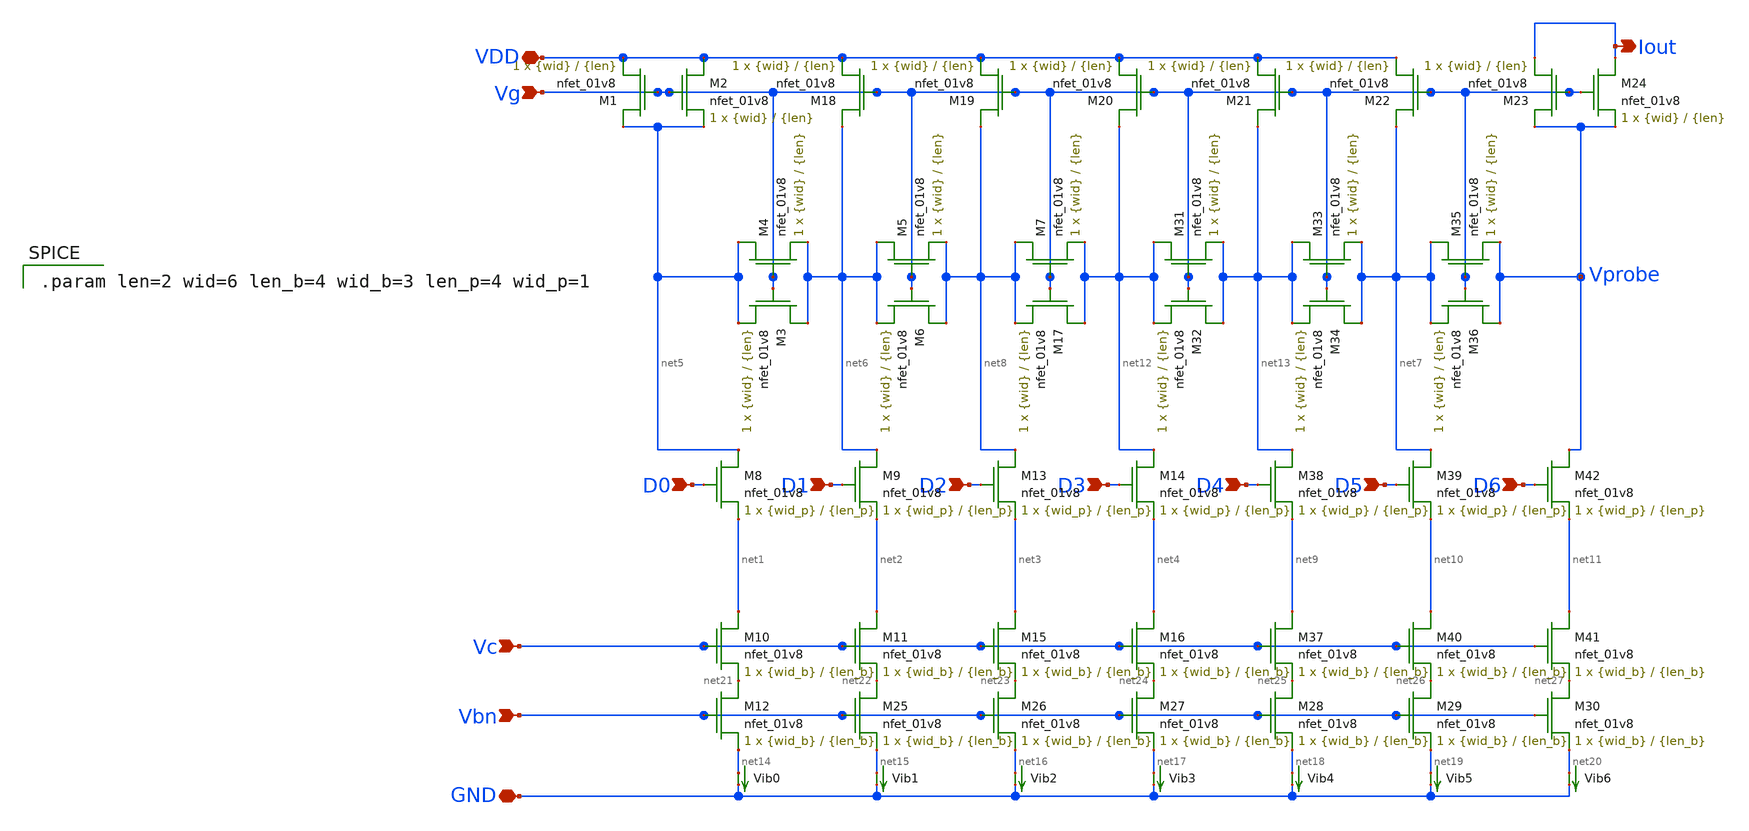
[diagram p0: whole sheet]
** sch_path: mp3/ladder.sch
**.subckt ladder Vbn VDD Iout GND D0 D1 D2 D3 D4 D5 D6 Vg Vc
*.ipin Vbn
*.iopin VDD
*.opin Iout
*.iopin GND
*.ipin D0
*.ipin D1
*.ipin D2
*.ipin D3
*.ipin D4
*.ipin D5
*.ipin D6
*.ipin Vg
*.ipin Vc
XM1 net5 Vg VDD GND sky130_fd_pr__nfet_01v8 L={len} W={wid} nf=1 ad='int((nf+1)/2) * W/nf * 0.29' as='int((nf+2)/2) * W/nf * 0.29'
+ pd='2*int((nf+1)/2) * (W/nf + 0.29)' ps='2*int((nf+2)/2) * (W/nf + 0.29)' nrd='0.29 / W' nrs='0.29 / W'
+ sa=0 sb=0 sd=0 mult=1 m=1
XM4 net5 Vg net6 GND sky130_fd_pr__nfet_01v8 L={len} W={wid} nf=1 ad='int((nf+1)/2) * W/nf * 0.29' as='int((nf+2)/2) * W/nf * 0.29'
+ pd='2*int((nf+1)/2) * (W/nf + 0.29)' ps='2*int((nf+2)/2) * (W/nf + 0.29)' nrd='0.29 / W' nrs='0.29 / W'
+ sa=0 sb=0 sd=0 mult=1 m=1
XM12 net21 Vbn net14 GND sky130_fd_pr__nfet_01v8 L={len_b} W={wid_b} nf=1 ad='int((nf+1)/2) * W/nf * 0.29'
+ as='int((nf+2)/2) * W/nf * 0.29' pd='2*int((nf+1)/2) * (W/nf + 0.29)' ps='2*int((nf+2)/2) * (W/nf + 0.29)'
+ nrd='0.29 / W' nrs='0.29 / W' sa=0 sb=0 sd=0 mult=1 m=1
XM2 VDD Vg net5 GND sky130_fd_pr__nfet_01v8 L={len} W={wid} nf=1 ad='int((nf+1)/2) * W/nf * 0.29' as='int((nf+2)/2) * W/nf * 0.29'
+ pd='2*int((nf+1)/2) * (W/nf + 0.29)' ps='2*int((nf+2)/2) * (W/nf + 0.29)' nrd='0.29 / W' nrs='0.29 / W'
+ sa=0 sb=0 sd=0 mult=1 m=1
XM18 net6 Vg VDD GND sky130_fd_pr__nfet_01v8 L={len} W={wid} nf=1 ad='int((nf+1)/2) * W/nf * 0.29' as='int((nf+2)/2) * W/nf * 0.29'
+ pd='2*int((nf+1)/2) * (W/nf + 0.29)' ps='2*int((nf+2)/2) * (W/nf + 0.29)' nrd='0.29 / W' nrs='0.29 / W'
+ sa=0 sb=0 sd=0 mult=1 m=1
XM19 net8 Vg VDD GND sky130_fd_pr__nfet_01v8 L={len} W={wid} nf=1 ad='int((nf+1)/2) * W/nf * 0.29' as='int((nf+2)/2) * W/nf * 0.29'
+ pd='2*int((nf+1)/2) * (W/nf + 0.29)' ps='2*int((nf+2)/2) * (W/nf + 0.29)' nrd='0.29 / W' nrs='0.29 / W'
+ sa=0 sb=0 sd=0 mult=1 m=1
XM20 net12 Vg VDD GND sky130_fd_pr__nfet_01v8 L={len} W={wid} nf=1 ad='int((nf+1)/2) * W/nf * 0.29' as='int((nf+2)/2) * W/nf * 0.29'
+ pd='2*int((nf+1)/2) * (W/nf + 0.29)' ps='2*int((nf+2)/2) * (W/nf + 0.29)' nrd='0.29 / W' nrs='0.29 / W'
+ sa=0 sb=0 sd=0 mult=1 m=1
XM21 net13 Vg VDD GND sky130_fd_pr__nfet_01v8 L={len} W={wid} nf=1 ad='int((nf+1)/2) * W/nf * 0.29' as='int((nf+2)/2) * W/nf * 0.29'
+ pd='2*int((nf+1)/2) * (W/nf + 0.29)' ps='2*int((nf+2)/2) * (W/nf + 0.29)' nrd='0.29 / W' nrs='0.29 / W'
+ sa=0 sb=0 sd=0 mult=1 m=1
XM22 net7 Vg VDD GND sky130_fd_pr__nfet_01v8 L={len} W={wid} nf=1 ad='int((nf+1)/2) * W/nf * 0.29' as='int((nf+2)/2) * W/nf * 0.29'
+ pd='2*int((nf+1)/2) * (W/nf + 0.29)' ps='2*int((nf+2)/2) * (W/nf + 0.29)' nrd='0.29 / W' nrs='0.29 / W'
+ sa=0 sb=0 sd=0 mult=1 m=1
XM23 Vprobe Vg Iout GND sky130_fd_pr__nfet_01v8 L={len} W={wid} nf=1 ad='int((nf+1)/2) * W/nf * 0.29'
+ as='int((nf+2)/2) * W/nf * 0.29' pd='2*int((nf+1)/2) * (W/nf + 0.29)' ps='2*int((nf+2)/2) * (W/nf + 0.29)'
+ nrd='0.29 / W' nrs='0.29 / W' sa=0 sb=0 sd=0 mult=1 m=1
XM24 Iout Vg Vprobe GND sky130_fd_pr__nfet_01v8 L={len} W={wid} nf=1 ad='int((nf+1)/2) * W/nf * 0.29'
+ as='int((nf+2)/2) * W/nf * 0.29' pd='2*int((nf+1)/2) * (W/nf + 0.29)' ps='2*int((nf+2)/2) * (W/nf + 0.29)'
+ nrd='0.29 / W' nrs='0.29 / W' sa=0 sb=0 sd=0 mult=1 m=1
XM3 net6 Vg net5 GND sky130_fd_pr__nfet_01v8 L={len} W={wid} nf=1 ad='int((nf+1)/2) * W/nf * 0.29' as='int((nf+2)/2) * W/nf * 0.29'
+ pd='2*int((nf+1)/2) * (W/nf + 0.29)' ps='2*int((nf+2)/2) * (W/nf + 0.29)' nrd='0.29 / W' nrs='0.29 / W'
+ sa=0 sb=0 sd=0 mult=1 m=1
XM5 net6 Vg net8 GND sky130_fd_pr__nfet_01v8 L={len} W={wid} nf=1 ad='int((nf+1)/2) * W/nf * 0.29' as='int((nf+2)/2) * W/nf * 0.29'
+ pd='2*int((nf+1)/2) * (W/nf + 0.29)' ps='2*int((nf+2)/2) * (W/nf + 0.29)' nrd='0.29 / W' nrs='0.29 / W'
+ sa=0 sb=0 sd=0 mult=1 m=1
XM6 net8 Vg net6 GND sky130_fd_pr__nfet_01v8 L={len} W={wid} nf=1 ad='int((nf+1)/2) * W/nf * 0.29' as='int((nf+2)/2) * W/nf * 0.29'
+ pd='2*int((nf+1)/2) * (W/nf + 0.29)' ps='2*int((nf+2)/2) * (W/nf + 0.29)' nrd='0.29 / W' nrs='0.29 / W'
+ sa=0 sb=0 sd=0 mult=1 m=1
XM7 net8 Vg net12 GND sky130_fd_pr__nfet_01v8 L={len} W={wid} nf=1 ad='int((nf+1)/2) * W/nf * 0.29' as='int((nf+2)/2) * W/nf * 0.29'
+ pd='2*int((nf+1)/2) * (W/nf + 0.29)' ps='2*int((nf+2)/2) * (W/nf + 0.29)' nrd='0.29 / W' nrs='0.29 / W'
+ sa=0 sb=0 sd=0 mult=1 m=1
XM17 net12 Vg net8 GND sky130_fd_pr__nfet_01v8 L={len} W={wid} nf=1 ad='int((nf+1)/2) * W/nf * 0.29'
+ as='int((nf+2)/2) * W/nf * 0.29' pd='2*int((nf+1)/2) * (W/nf + 0.29)' ps='2*int((nf+2)/2) * (W/nf + 0.29)'
+ nrd='0.29 / W' nrs='0.29 / W' sa=0 sb=0 sd=0 mult=1 m=1
XM31 net12 Vg net13 GND sky130_fd_pr__nfet_01v8 L={len} W={wid} nf=1 ad='int((nf+1)/2) * W/nf * 0.29'
+ as='int((nf+2)/2) * W/nf * 0.29' pd='2*int((nf+1)/2) * (W/nf + 0.29)' ps='2*int((nf+2)/2) * (W/nf + 0.29)'
+ nrd='0.29 / W' nrs='0.29 / W' sa=0 sb=0 sd=0 mult=1 m=1
XM32 net13 Vg net12 GND sky130_fd_pr__nfet_01v8 L={len} W={wid} nf=1 ad='int((nf+1)/2) * W/nf * 0.29'
+ as='int((nf+2)/2) * W/nf * 0.29' pd='2*int((nf+1)/2) * (W/nf + 0.29)' ps='2*int((nf+2)/2) * (W/nf + 0.29)'
+ nrd='0.29 / W' nrs='0.29 / W' sa=0 sb=0 sd=0 mult=1 m=1
XM33 net13 Vg net7 GND sky130_fd_pr__nfet_01v8 L={len} W={wid} nf=1 ad='int((nf+1)/2) * W/nf * 0.29'
+ as='int((nf+2)/2) * W/nf * 0.29' pd='2*int((nf+1)/2) * (W/nf + 0.29)' ps='2*int((nf+2)/2) * (W/nf + 0.29)'
+ nrd='0.29 / W' nrs='0.29 / W' sa=0 sb=0 sd=0 mult=1 m=1
XM34 net7 Vg net13 GND sky130_fd_pr__nfet_01v8 L={len} W={wid} nf=1 ad='int((nf+1)/2) * W/nf * 0.29'
+ as='int((nf+2)/2) * W/nf * 0.29' pd='2*int((nf+1)/2) * (W/nf + 0.29)' ps='2*int((nf+2)/2) * (W/nf + 0.29)'
+ nrd='0.29 / W' nrs='0.29 / W' sa=0 sb=0 sd=0 mult=1 m=1
XM35 net7 Vg Vprobe GND sky130_fd_pr__nfet_01v8 L={len} W={wid} nf=1 ad='int((nf+1)/2) * W/nf * 0.29'
+ as='int((nf+2)/2) * W/nf * 0.29' pd='2*int((nf+1)/2) * (W/nf + 0.29)' ps='2*int((nf+2)/2) * (W/nf + 0.29)'
+ nrd='0.29 / W' nrs='0.29 / W' sa=0 sb=0 sd=0 mult=1 m=1
XM36 Vprobe Vg net7 GND sky130_fd_pr__nfet_01v8 L={len} W={wid} nf=1 ad='int((nf+1)/2) * W/nf * 0.29'
+ as='int((nf+2)/2) * W/nf * 0.29' pd='2*int((nf+1)/2) * (W/nf + 0.29)' ps='2*int((nf+2)/2) * (W/nf + 0.29)'
+ nrd='0.29 / W' nrs='0.29 / W' sa=0 sb=0 sd=0 mult=1 m=1
Vib0 net14 GND 0
.save i(vib0)
Vib1 net15 GND 0
.save i(vib1)
Vib2 net16 GND 0
.save i(vib2)
Vib3 net17 GND 0
.save i(vib3)
Vib4 net18 GND 0
.save i(vib4)
Vib5 net19 GND 0
.save i(vib5)
Vib6 net20 GND 0
.save i(vib6)
XM8 net5 D0 net1 GND sky130_fd_pr__nfet_01v8 L={len_p} W={wid_p} nf=1 ad='int((nf+1)/2) * W/nf * 0.29'
+ as='int((nf+2)/2) * W/nf * 0.29' pd='2*int((nf+1)/2) * (W/nf + 0.29)' ps='2*int((nf+2)/2) * (W/nf + 0.29)'
+ nrd='0.29 / W' nrs='0.29 / W' sa=0 sb=0 sd=0 mult=1 m=1
XM9 net6 D1 net2 GND sky130_fd_pr__nfet_01v8 L={len_p} W={wid_p} nf=1 ad='int((nf+1)/2) * W/nf * 0.29'
+ as='int((nf+2)/2) * W/nf * 0.29' pd='2*int((nf+1)/2) * (W/nf + 0.29)' ps='2*int((nf+2)/2) * (W/nf + 0.29)'
+ nrd='0.29 / W' nrs='0.29 / W' sa=0 sb=0 sd=0 mult=1 m=1
XM13 net8 D2 net3 GND sky130_fd_pr__nfet_01v8 L={len_p} W={wid_p} nf=1 ad='int((nf+1)/2) * W/nf * 0.29'
+ as='int((nf+2)/2) * W/nf * 0.29' pd='2*int((nf+1)/2) * (W/nf + 0.29)' ps='2*int((nf+2)/2) * (W/nf + 0.29)'
+ nrd='0.29 / W' nrs='0.29 / W' sa=0 sb=0 sd=0 mult=1 m=1
XM14 net12 D3 net4 GND sky130_fd_pr__nfet_01v8 L={len_p} W={wid_p} nf=1 ad='int((nf+1)/2) * W/nf * 0.29'
+ as='int((nf+2)/2) * W/nf * 0.29' pd='2*int((nf+1)/2) * (W/nf + 0.29)' ps='2*int((nf+2)/2) * (W/nf + 0.29)'
+ nrd='0.29 / W' nrs='0.29 / W' sa=0 sb=0 sd=0 mult=1 m=1
XM38 net13 D4 net9 GND sky130_fd_pr__nfet_01v8 L={len_p} W={wid_p} nf=1 ad='int((nf+1)/2) * W/nf * 0.29'
+ as='int((nf+2)/2) * W/nf * 0.29' pd='2*int((nf+1)/2) * (W/nf + 0.29)' ps='2*int((nf+2)/2) * (W/nf + 0.29)'
+ nrd='0.29 / W' nrs='0.29 / W' sa=0 sb=0 sd=0 mult=1 m=1
XM39 net7 D5 net10 GND sky130_fd_pr__nfet_01v8 L={len_p} W={wid_p} nf=1 ad='int((nf+1)/2) * W/nf * 0.29'
+ as='int((nf+2)/2) * W/nf * 0.29' pd='2*int((nf+1)/2) * (W/nf + 0.29)' ps='2*int((nf+2)/2) * (W/nf + 0.29)'
+ nrd='0.29 / W' nrs='0.29 / W' sa=0 sb=0 sd=0 mult=1 m=1
XM42 Vprobe D6 net11 GND sky130_fd_pr__nfet_01v8 L={len_p} W={wid_p} nf=1 ad='int((nf+1)/2) * W/nf * 0.29'
+ as='int((nf+2)/2) * W/nf * 0.29' pd='2*int((nf+1)/2) * (W/nf + 0.29)' ps='2*int((nf+2)/2) * (W/nf + 0.29)'
+ nrd='0.29 / W' nrs='0.29 / W' sa=0 sb=0 sd=0 mult=1 m=1
XM25 net22 Vbn net15 GND sky130_fd_pr__nfet_01v8 L={len_b} W={wid_b} nf=1 ad='int((nf+1)/2) * W/nf * 0.29'
+ as='int((nf+2)/2) * W/nf * 0.29' pd='2*int((nf+1)/2) * (W/nf + 0.29)' ps='2*int((nf+2)/2) * (W/nf + 0.29)'
+ nrd='0.29 / W' nrs='0.29 / W' sa=0 sb=0 sd=0 mult=1 m=1
XM26 net23 Vbn net16 GND sky130_fd_pr__nfet_01v8 L={len_b} W={wid_b} nf=1 ad='int((nf+1)/2) * W/nf * 0.29'
+ as='int((nf+2)/2) * W/nf * 0.29' pd='2*int((nf+1)/2) * (W/nf + 0.29)' ps='2*int((nf+2)/2) * (W/nf + 0.29)'
+ nrd='0.29 / W' nrs='0.29 / W' sa=0 sb=0 sd=0 mult=1 m=1
XM27 net24 Vbn net17 GND sky130_fd_pr__nfet_01v8 L={len_b} W={wid_b} nf=1 ad='int((nf+1)/2) * W/nf * 0.29'
+ as='int((nf+2)/2) * W/nf * 0.29' pd='2*int((nf+1)/2) * (W/nf + 0.29)' ps='2*int((nf+2)/2) * (W/nf + 0.29)'
+ nrd='0.29 / W' nrs='0.29 / W' sa=0 sb=0 sd=0 mult=1 m=1
XM28 net25 Vbn net18 GND sky130_fd_pr__nfet_01v8 L={len_b} W={wid_b} nf=1 ad='int((nf+1)/2) * W/nf * 0.29'
+ as='int((nf+2)/2) * W/nf * 0.29' pd='2*int((nf+1)/2) * (W/nf + 0.29)' ps='2*int((nf+2)/2) * (W/nf + 0.29)'
+ nrd='0.29 / W' nrs='0.29 / W' sa=0 sb=0 sd=0 mult=1 m=1
XM29 net26 Vbn net19 GND sky130_fd_pr__nfet_01v8 L={len_b} W={wid_b} nf=1 ad='int((nf+1)/2) * W/nf * 0.29'
+ as='int((nf+2)/2) * W/nf * 0.29' pd='2*int((nf+1)/2) * (W/nf + 0.29)' ps='2*int((nf+2)/2) * (W/nf + 0.29)'
+ nrd='0.29 / W' nrs='0.29 / W' sa=0 sb=0 sd=0 mult=1 m=1
XM30 net27 Vbn net20 GND sky130_fd_pr__nfet_01v8 L={len_b} W={wid_b} nf=1 ad='int((nf+1)/2) * W/nf * 0.29'
+ as='int((nf+2)/2) * W/nf * 0.29' pd='2*int((nf+1)/2) * (W/nf + 0.29)' ps='2*int((nf+2)/2) * (W/nf + 0.29)'
+ nrd='0.29 / W' nrs='0.29 / W' sa=0 sb=0 sd=0 mult=1 m=1
XM10 net1 Vc net21 GND sky130_fd_pr__nfet_01v8 L={len_b} W={wid_b} nf=1 ad='int((nf+1)/2) * W/nf * 0.29'
+ as='int((nf+2)/2) * W/nf * 0.29' pd='2*int((nf+1)/2) * (W/nf + 0.29)' ps='2*int((nf+2)/2) * (W/nf + 0.29)'
+ nrd='0.29 / W' nrs='0.29 / W' sa=0 sb=0 sd=0 mult=1 m=1
XM11 net2 Vc net22 GND sky130_fd_pr__nfet_01v8 L={len_b} W={wid_b} nf=1 ad='int((nf+1)/2) * W/nf * 0.29'
+ as='int((nf+2)/2) * W/nf * 0.29' pd='2*int((nf+1)/2) * (W/nf + 0.29)' ps='2*int((nf+2)/2) * (W/nf + 0.29)'
+ nrd='0.29 / W' nrs='0.29 / W' sa=0 sb=0 sd=0 mult=1 m=1
XM15 net3 Vc net23 GND sky130_fd_pr__nfet_01v8 L={len_b} W={wid_b} nf=1 ad='int((nf+1)/2) * W/nf * 0.29'
+ as='int((nf+2)/2) * W/nf * 0.29' pd='2*int((nf+1)/2) * (W/nf + 0.29)' ps='2*int((nf+2)/2) * (W/nf + 0.29)'
+ nrd='0.29 / W' nrs='0.29 / W' sa=0 sb=0 sd=0 mult=1 m=1
XM16 net4 Vc net24 GND sky130_fd_pr__nfet_01v8 L={len_b} W={wid_b} nf=1 ad='int((nf+1)/2) * W/nf * 0.29'
+ as='int((nf+2)/2) * W/nf * 0.29' pd='2*int((nf+1)/2) * (W/nf + 0.29)' ps='2*int((nf+2)/2) * (W/nf + 0.29)'
+ nrd='0.29 / W' nrs='0.29 / W' sa=0 sb=0 sd=0 mult=1 m=1
XM37 net9 Vc net25 GND sky130_fd_pr__nfet_01v8 L={len_b} W={wid_b} nf=1 ad='int((nf+1)/2) * W/nf * 0.29'
+ as='int((nf+2)/2) * W/nf * 0.29' pd='2*int((nf+1)/2) * (W/nf + 0.29)' ps='2*int((nf+2)/2) * (W/nf + 0.29)'
+ nrd='0.29 / W' nrs='0.29 / W' sa=0 sb=0 sd=0 mult=1 m=1
XM40 net10 Vc net26 GND sky130_fd_pr__nfet_01v8 L={len_b} W={wid_b} nf=1 ad='int((nf+1)/2) * W/nf * 0.29'
+ as='int((nf+2)/2) * W/nf * 0.29' pd='2*int((nf+1)/2) * (W/nf + 0.29)' ps='2*int((nf+2)/2) * (W/nf + 0.29)'
+ nrd='0.29 / W' nrs='0.29 / W' sa=0 sb=0 sd=0 mult=1 m=1
XM41 net11 Vc net27 GND sky130_fd_pr__nfet_01v8 L={len_b} W={wid_b} nf=1 ad='int((nf+1)/2) * W/nf * 0.29'
+ as='int((nf+2)/2) * W/nf * 0.29' pd='2*int((nf+1)/2) * (W/nf + 0.29)' ps='2*int((nf+2)/2) * (W/nf + 0.29)'
+ nrd='0.29 / W' nrs='0.29 / W' sa=0 sb=0 sd=0 mult=1 m=1
**** begin user architecture code

.param len=2 wid=6 len_b=4 wid_b=3 len_p=4 wid_p=1

**** end user architecture code
**.ends
.end
